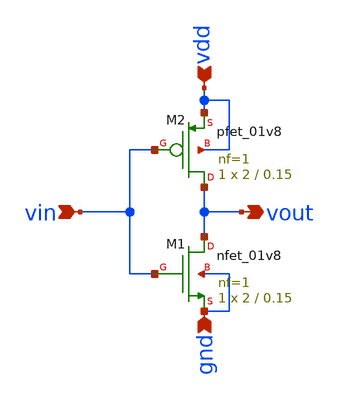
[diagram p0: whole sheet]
** sch_path: 04 - VTC Analysis/inv_vtc.sch
**.subckt inv_vtc vin gnd vdd vout
*.ipin vin
*.ipin gnd
*.ipin vdd
*.opin vout
XM1 vout vin gnd gnd sky130_fd_pr__nfet_01v8 L=0.15 W=2 nf=1 ad='int((nf+1)/2) * W/nf * 0.29' as='int((nf+2)/2) * W/nf * 0.29'
+ pd='2*int((nf+1)/2) * (W/nf + 0.29)' ps='2*int((nf+2)/2) * (W/nf + 0.29)' nrd='0.29 / W' nrs='0.29 / W'
+ sa=0 sb=0 sd=0 mult=1 m=1
XM2 vout vin vdd vdd sky130_fd_pr__pfet_01v8 L=0.15 W=2 nf=1 ad='int((nf+1)/2) * W/nf * 0.29' as='int((nf+2)/2) * W/nf * 0.29'
+ pd='2*int((nf+1)/2) * (W/nf + 0.29)' ps='2*int((nf+2)/2) * (W/nf + 0.29)' nrd='0.29 / W' nrs='0.29 / W'
+ sa=0 sb=0 sd=0 mult=1 m=1
**.ends
.end
